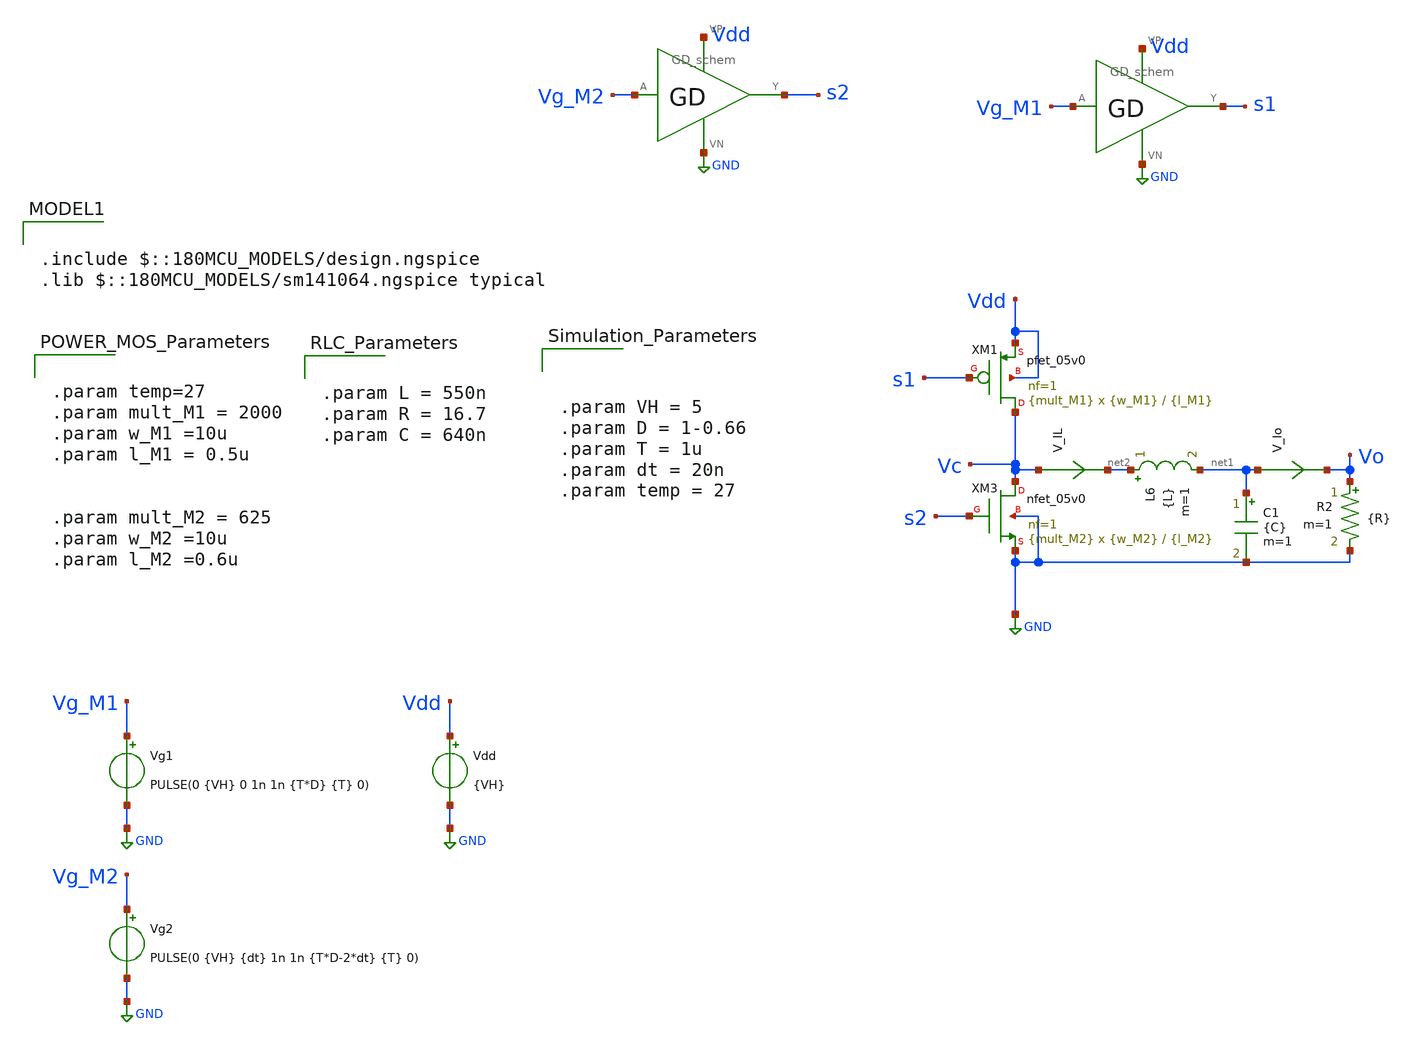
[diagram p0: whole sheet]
** sch_path: xschem/pwr_stage/TB_DCDCBuck_GD_FR_2.sch
**.subckt TB_DCDCBuck_GD_FR_2
Vdd Vdd GND {VH}
Vg2 Vg_M2 GND PULSE(0 {VH} {dt} 1n 1n {T*D-2*dt} {T} 0)
Vg1 Vg_M1 GND PULSE(0 {VH} 0 1n 1n {T*D} {T} 0)
L6 net2 net1 {L} m=1
C1 net1 GND {C} m=1
V_Io net1 Vo 0
.save i(v_io)
V_IL Vc net2 0
.save i(v_il)
R2 Vo GND {R} m=1
XM3 Vc s2 GND GND nfet_05v0 L={l_M2} W={w_M2} nf=1 ad='int((nf+1)/2) * W/nf * 0.18u' as='int((nf+2)/2) * W/nf * 0.18u'
+ pd='2*int((nf+1)/2) * (W/nf + 0.18u)' ps='2*int((nf+2)/2) * (W/nf + 0.18u)' nrd='0.18u / W' nrs='0.18u / W'
+ sa=0 sb=0 sd=0 m={mult_M2}
XM1 Vc s1 Vdd Vdd pfet_05v0 L={l_M1} W={w_M1} nf=1 ad='int((nf+1)/2) * W/nf * 0.18u' as='int((nf+2)/2) * W/nf * 0.18u'
+ pd='2*int((nf+1)/2) * (W/nf + 0.18u)' ps='2*int((nf+2)/2) * (W/nf + 0.18u)' nrd='0.18u / W' nrs='0.18u / W'
+ sa=0 sb=0 sd=0 m={mult_M1}
X1 Vdd GND Vg_M2 s2 GD_schem
X2 Vdd GND Vg_M1 s1 GD_schem
**** begin user architecture code


.param L = 550n
.param R = 16.7
.param C = 640n





.param temp=27
.param mult_M1 = 2000
.param w_M1 =10u
.param l_M1 = 0.5u


.param mult_M2 = 625
.param w_M2 =10u
.param l_M2 =0.6u









.param VH = 5
.param D = 1-0.66
.param T = 1u
.param dt = 20n
.param temp = 27






.save all
.ic v(vo) = 0
.control
set color0 = white
compose RL_var values 3.3/0.05 3.3/0.1 3.3/0.25 3.3/0.5 3.3/0.7 3.3 3.3/3
   foreach val $&RL_var
     alterparam R=$val
     reset
     save i(V_Io) v(Vo) i(Vdd) v(Vdd)
     tran 100p 30u 20u
   end
wrdata /foss/designs/data_Chipathon_2025/data_converter_700mA_GD_100p.txt tran1.i(V_Io) tran1.v(Vo)
+ tran1.i(Vdd) tran1.v(Vdd) tran2.i(V_Io) tran2.v(Vo) tran2.i(Vdd) tran2.v(Vdd) tran3.i(V_Io) tran3.v(Vo)
+ tran3.i(Vdd) tran3.v(Vdd) tran4.i(V_Io) tran4.v(Vo) tran4.i(Vdd) tran4.v(Vdd) tran5.i(V_Io) tran5.v(Vo)
+ tran5.i(Vdd) tran5.v(Vdd) tran6.i(V_Io) tran6.v(Vo) tran6.i(Vdd) tran6.v(Vdd) tran7.i(V_Io) tran7.v(Vo)
+ tran7.i(Vdd) tran7.v(Vdd)
.endc
.end



.include $::180MCU_MODELS/design.ngspice
.lib $::180MCU_MODELS/sm141064.ngspice typical




*PMOS
.param mult_gd_p = 72
.param w_gd_p = 6.4u
.param l_gd_p = 0.5u
*NMOS
.param mult_gd_n = 72
.param w_gd_n = 2u
.param l_gd_n = 0.6u



**** end user architecture code
**.ends

* expanding   symbol:  pwr_stage/GD_schem.sym # of pins=4
** sym_path: xschem/pwr_stage/GD_schem.sym
** sch_path: xschem/pwr_stage/GD_schem.sch
.subckt GD_schem VP VN A Y
*.ipin A
*.iopin VP
*.iopin VN
*.opin Y
XM11 Y net1 VN VN nfet_05v0 L={l_gd_n} W={w_gd_n} nf=1 ad='int((nf+1)/2) * W/nf * 0.18u' as='int((nf+2)/2) * W/nf * 0.18u'
+ pd='2*int((nf+1)/2) * (W/nf + 0.18u)' ps='2*int((nf+2)/2) * (W/nf + 0.18u)' nrd='0.18u / W' nrs='0.18u / W'
+ sa=0 sb=0 sd=0 m={mult_gd_n}
XM12 Y net1 VP VP pfet_05v0 L={l_gd_p} W={w_gd_p} nf=1 ad='int((nf+1)/2) * W/nf * 0.18u' as='int((nf+2)/2) * W/nf * 0.18u'
+ pd='2*int((nf+1)/2) * (W/nf + 0.18u)' ps='2*int((nf+2)/2) * (W/nf + 0.18u)' nrd='0.18u / W' nrs='0.18u / W'
+ sa=0 sb=0 sd=0 m={mult_gd_p}
XM13 net1 A VN VN nfet_05v0 L={l_gd_n} W={w_gd_n} nf=1 ad='int((nf+1)/2) * W/nf * 0.18u' as='int((nf+2)/2) * W/nf * 0.18u'
+ pd='2*int((nf+1)/2) * (W/nf + 0.18u)' ps='2*int((nf+2)/2) * (W/nf + 0.18u)' nrd='0.18u / W' nrs='0.18u / W'
+ sa=0 sb=0 sd=0 m={mult_gd_n}/4
XM14 net1 A VP VP pfet_05v0 L={l_gd_p} W={w_gd_p} nf=1 ad='int((nf+1)/2) * W/nf * 0.18u' as='int((nf+2)/2) * W/nf * 0.18u'
+ pd='2*int((nf+1)/2) * (W/nf + 0.18u)' ps='2*int((nf+2)/2) * (W/nf + 0.18u)' nrd='0.18u / W' nrs='0.18u / W'
+ sa=0 sb=0 sd=0 m={mult_gd_p}/4
.ends

.GLOBAL GND
.end
